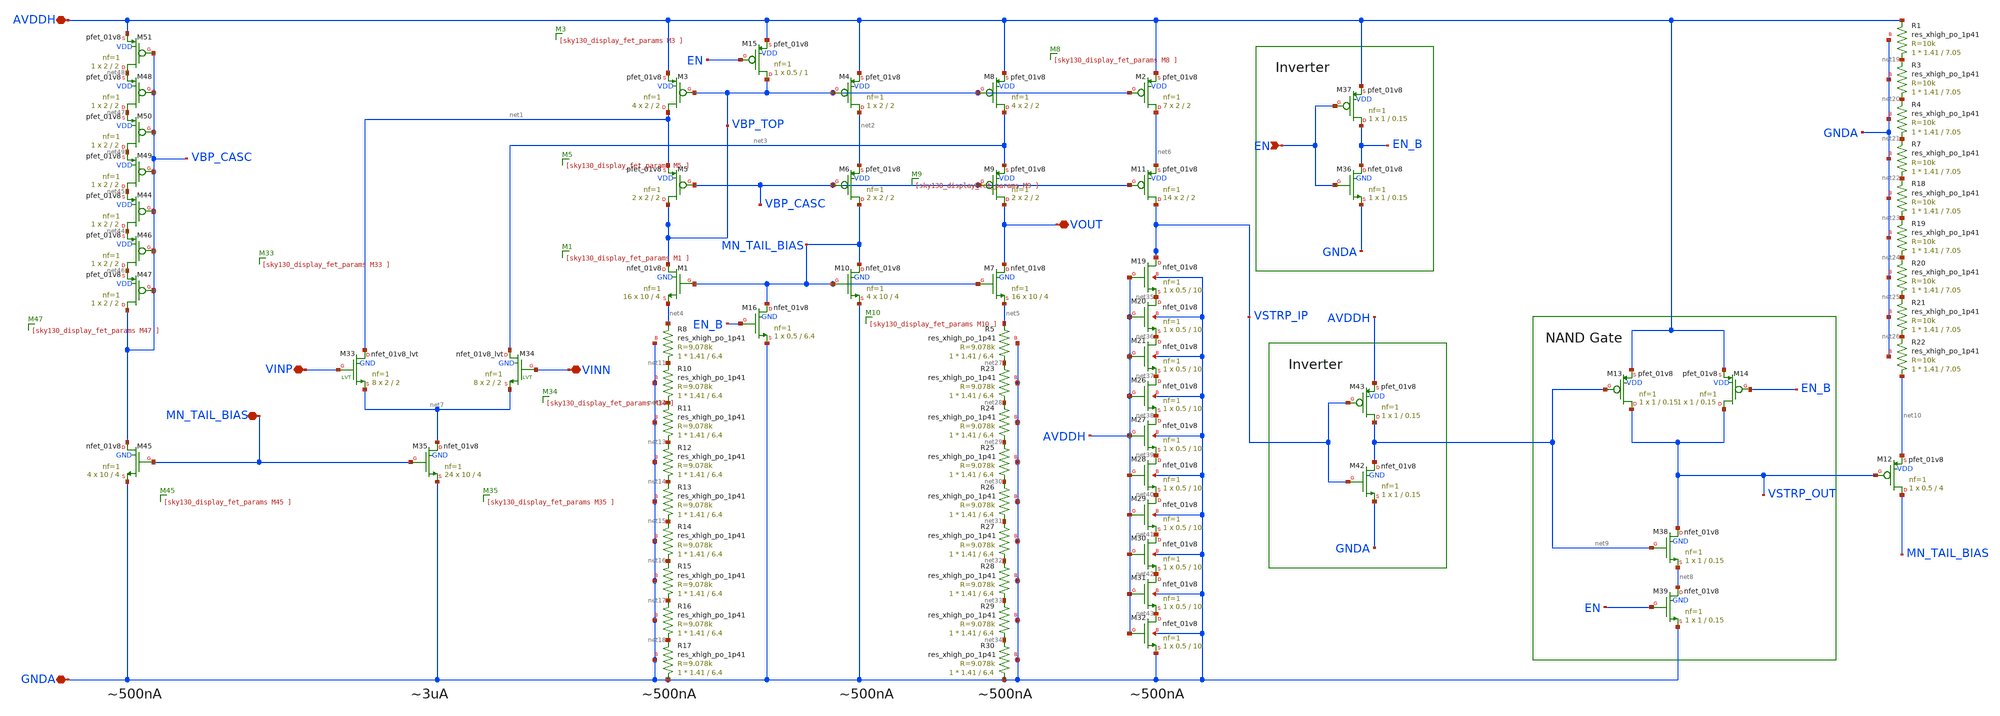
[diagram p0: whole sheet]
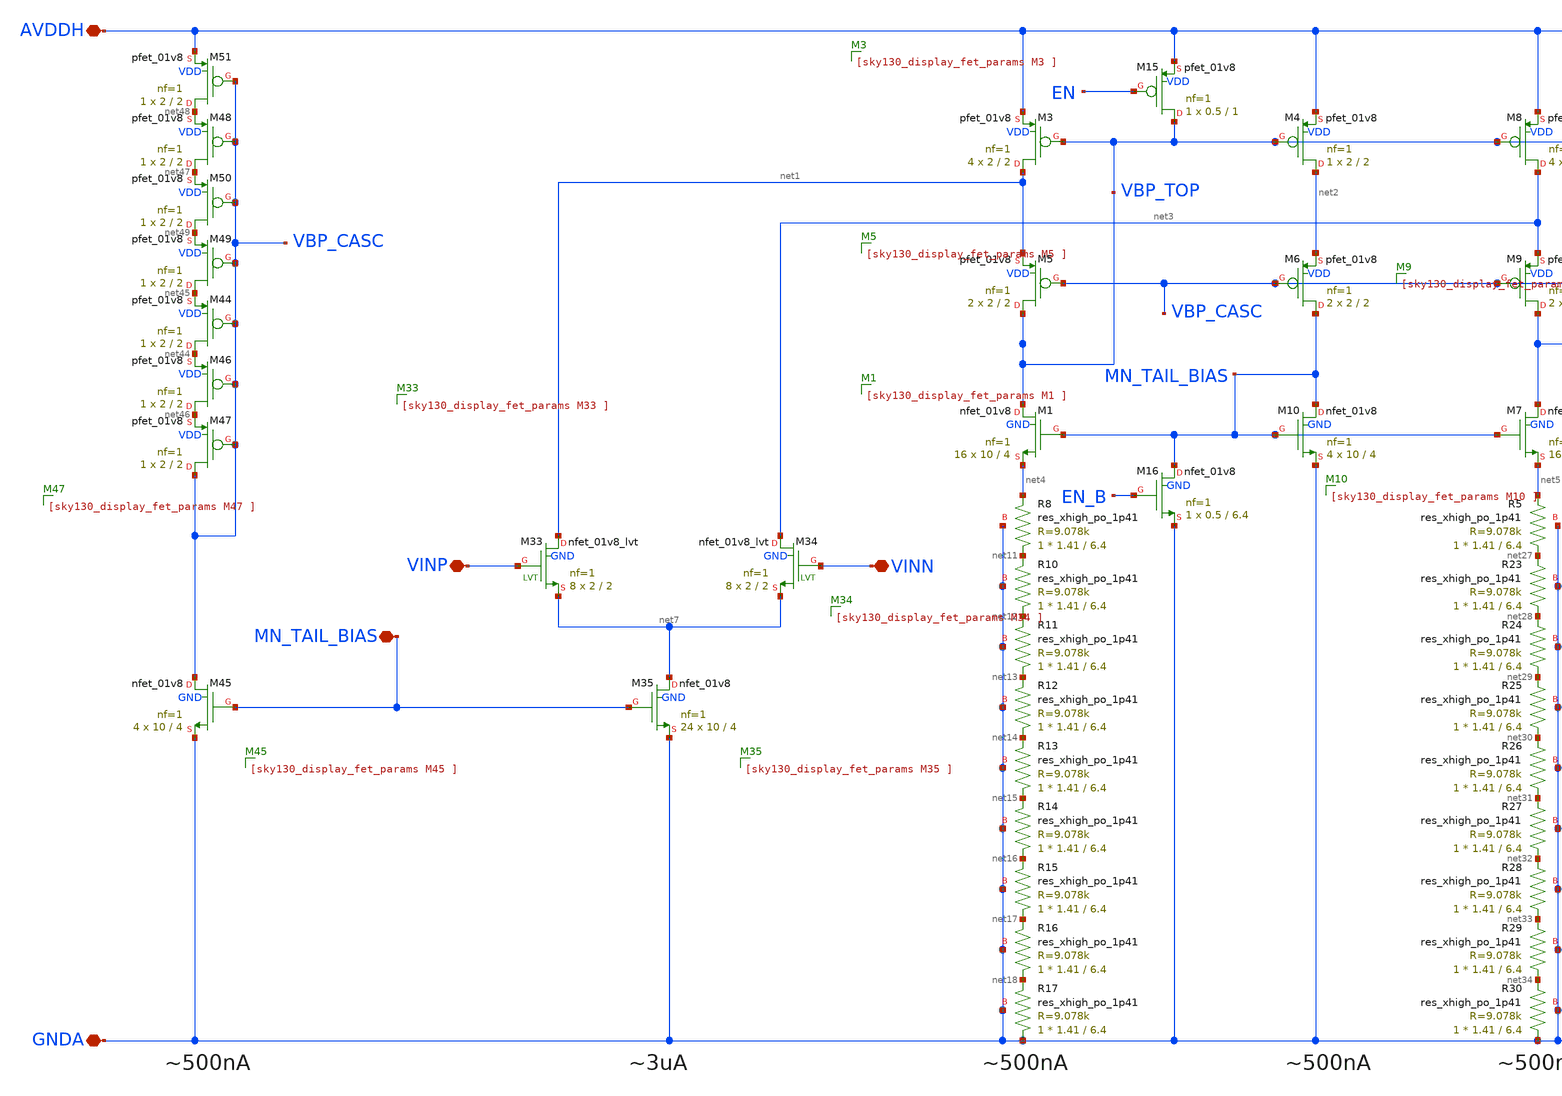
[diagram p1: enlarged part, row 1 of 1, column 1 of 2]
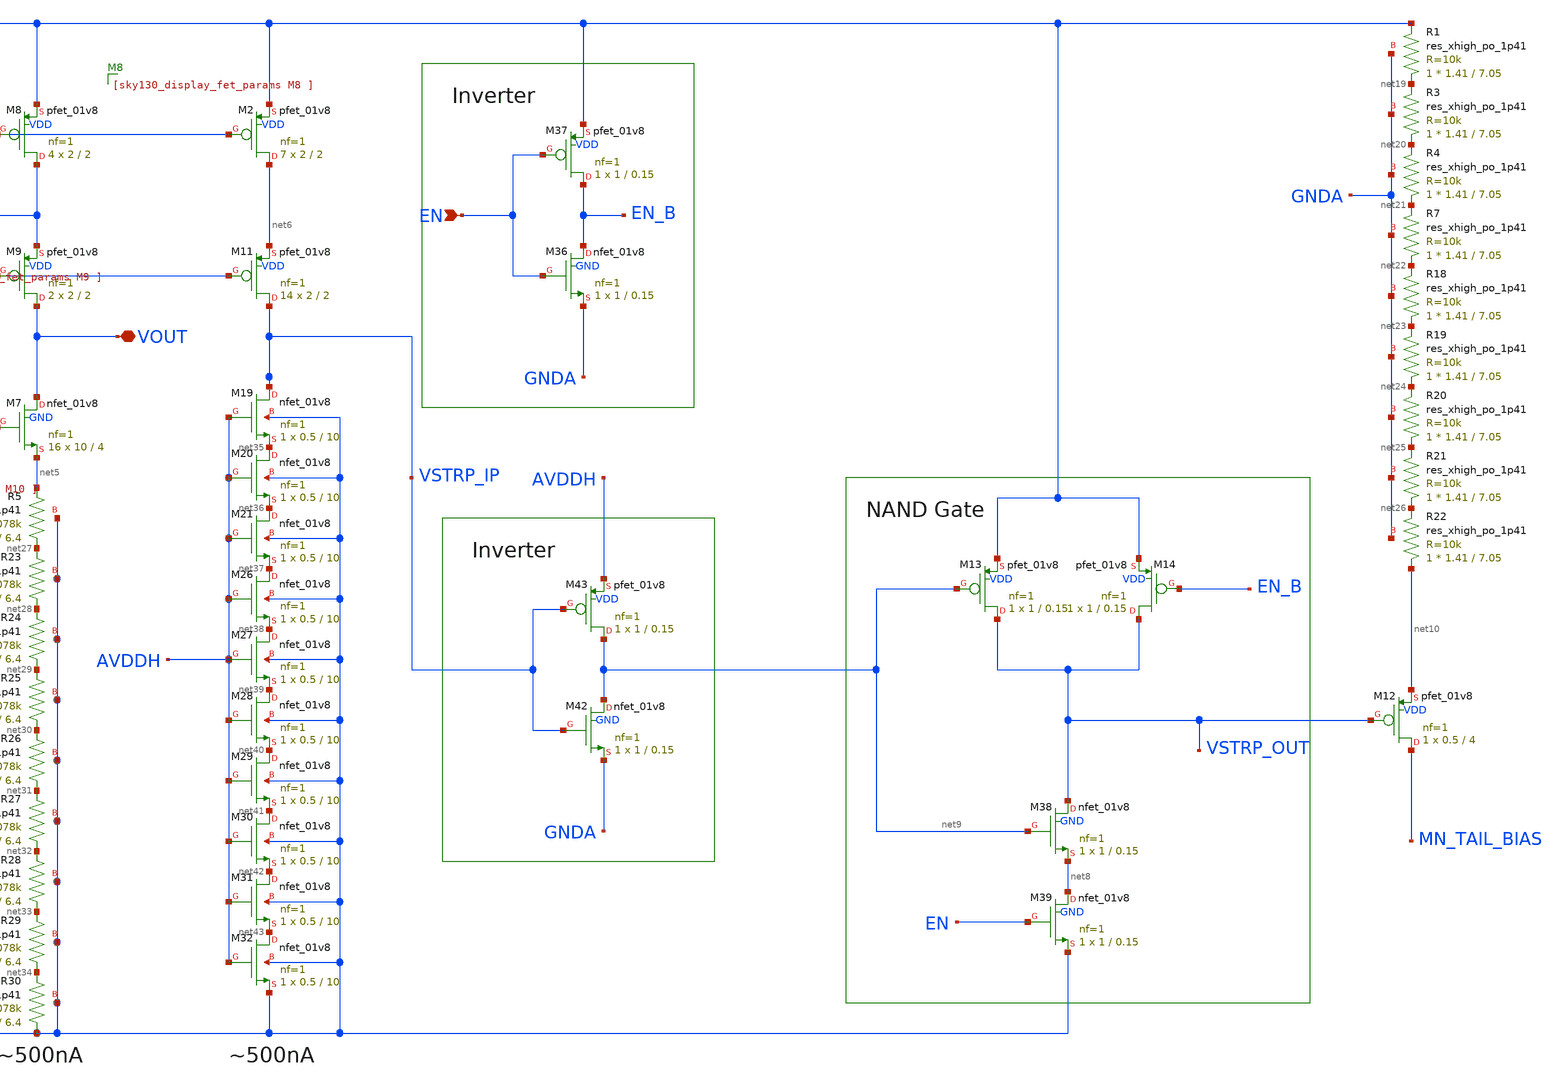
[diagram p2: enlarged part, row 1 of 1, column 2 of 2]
** sch_path: OTAs/NMOS_FoldedCasc_SE_OTA_IntBias/SCH/OTA_Gm_Cell_v2.sch
**.subckt OTA_Gm_Cell_v2 AVDDH GNDA VOUT MN_TAIL_BIAS EN VINP VINN
*.iopin AVDDH
*.iopin GNDA
*.iopin VOUT
*.iopin MN_TAIL_BIAS
*.ipin EN
*.iopin VINP
*.iopin VINN
XM1 VBP_TOP MN_TAIL_BIAS net4 GND sky130_fd_pr__nfet_01v8 L=4 W=10 nf=1 ad='int((1 + 1)/2) * 10 / 1 * 0.29'
+ as='int((1 + 2)/2) * 10 / 1 * 0.29' pd='2*int((1 + 1)/2) * (10 / 1 + 0.29)' ps='2*int((1 + 2)/2) * (10 / 1 + 0.29)'
+ nrd='0.29 / 10 ' nrs='0.29 / 10 ' sa=0 sb=0 sd=0 mult=16 m=16
XM3 net1 VBP_TOP AVDDH VDD sky130_fd_pr__pfet_01v8 L=2 W=2 nf=1 ad='int((1 + 1)/2) * 2 / 1 * 0.29' as='int((1 + 2)/2) * 2 / 1 * 0.29'
+ pd='2*int((1 + 1)/2) * (2 / 1 + 0.29)' ps='2*int((1 + 2)/2) * (2 / 1 + 0.29)' nrd='0.29 / 2 ' nrs='0.29 / 2 '
+ sa=0 sb=0 sd=0 mult=4 m=4
XM4 net2 VBP_TOP AVDDH VDD sky130_fd_pr__pfet_01v8 L=2 W=2 nf=1 ad='int((1 + 1)/2) * 2 / 1 * 0.29' as='int((1 + 2)/2) * 2 / 1 * 0.29'
+ pd='2*int((1 + 1)/2) * (2 / 1 + 0.29)' ps='2*int((1 + 2)/2) * (2 / 1 + 0.29)' nrd='0.29 / 2 ' nrs='0.29 / 2 '
+ sa=0 sb=0 sd=0 mult=1 m=1
XM5 VBP_TOP VBP_CASC net1 VDD sky130_fd_pr__pfet_01v8 L=2 W=2 nf=1 ad='int((1 + 1)/2) * 2 / 1 * 0.29'
+ as='int((1 + 2)/2) * 2 / 1 * 0.29' pd='2*int((1 + 1)/2) * (2 / 1 + 0.29)' ps='2*int((1 + 2)/2) * (2 / 1 + 0.29)'
+ nrd='0.29 / 2 ' nrs='0.29 / 2 ' sa=0 sb=0 sd=0 mult=2 m=2
XM6 MN_TAIL_BIAS VBP_CASC net2 VDD sky130_fd_pr__pfet_01v8 L=2 W=2 nf=1 ad='int((1 + 1)/2) * 2 / 1 * 0.29'
+ as='int((1 + 2)/2) * 2 / 1 * 0.29' pd='2*int((1 + 1)/2) * (2 / 1 + 0.29)' ps='2*int((1 + 2)/2) * (2 / 1 + 0.29)'
+ nrd='0.29 / 2 ' nrs='0.29 / 2 ' sa=0 sb=0 sd=0 mult=2 m=2
XM7 VOUT MN_TAIL_BIAS net5 GND sky130_fd_pr__nfet_01v8 L=4 W=10 nf=1 ad='int((1 + 1)/2) * 10 / 1 * 0.29'
+ as='int((1 + 2)/2) * 10 / 1 * 0.29' pd='2*int((1 + 1)/2) * (10 / 1 + 0.29)' ps='2*int((1 + 2)/2) * (10 / 1 + 0.29)'
+ nrd='0.29 / 10 ' nrs='0.29 / 10 ' sa=0 sb=0 sd=0 mult=16 m=16
XM10 MN_TAIL_BIAS MN_TAIL_BIAS GNDA GND sky130_fd_pr__nfet_01v8 L=4 W=10 nf=1 ad='int((1 + 1)/2) * 10 / 1 * 0.29'
+ as='int((1 + 2)/2) * 10 / 1 * 0.29' pd='2*int((1 + 1)/2) * (10 / 1 + 0.29)' ps='2*int((1 + 2)/2) * (10 / 1 + 0.29)'
+ nrd='0.29 / 10 ' nrs='0.29 / 10 ' sa=0 sb=0 sd=0 mult=4 m=4
XM12 MN_TAIL_BIAS VSTRP_OUT net10 VDD sky130_fd_pr__pfet_01v8 L=4 W=0.5 nf=1 ad='int((1 + 1)/2) * 0.5 / 1 * 0.29'
+ as='int((1 + 2)/2) * 0.5 / 1 * 0.29' pd='2*int((1 + 1)/2) * (0.5 / 1 + 0.29)' ps='2*int((1 + 2)/2) * (0.5 / 1 + 0.29)'
+ nrd='0.29 / 0.5 ' nrs='0.29 / 0.5 ' sa=0 sb=0 sd=0 mult=1 m=1
XM15 VBP_TOP EN AVDDH VDD sky130_fd_pr__pfet_01v8 L=1 W=0.5 nf=1 ad='int((1 + 1)/2) * 0.5 / 1 * 0.29'
+ as='int((1 + 2)/2) * 0.5 / 1 * 0.29' pd='2*int((1 + 1)/2) * (0.5 / 1 + 0.29)' ps='2*int((1 + 2)/2) * (0.5 / 1 + 0.29)'
+ nrd='0.29 / 0.5 ' nrs='0.29 / 0.5 ' sa=0 sb=0 sd=0 mult=1 m=1
XM16 MN_TAIL_BIAS EN_B GNDA GND sky130_fd_pr__nfet_01v8 L=6.4 W=0.5 nf=1 ad='int((1 + 1)/2) * 0.5 / 1 * 0.29'
+ as='int((1 + 2)/2) * 0.5 / 1 * 0.29' pd='2*int((1 + 1)/2) * (0.5 / 1 + 0.29)' ps='2*int((1 + 2)/2) * (0.5 / 1 + 0.29)'
+ nrd='0.29 / 0.5 ' nrs='0.29 / 0.5 ' sa=0 sb=0 sd=0 mult=1 m=1
XM8 net3 VBP_TOP AVDDH VDD sky130_fd_pr__pfet_01v8 L=2 W=2 nf=1 ad='int((1 + 1)/2) * 2 / 1 * 0.29' as='int((1 + 2)/2) * 2 / 1 * 0.29'
+ pd='2*int((1 + 1)/2) * (2 / 1 + 0.29)' ps='2*int((1 + 2)/2) * (2 / 1 + 0.29)' nrd='0.29 / 2 ' nrs='0.29 / 2 '
+ sa=0 sb=0 sd=0 mult=4 m=4
XM9 VOUT VBP_CASC net3 VDD sky130_fd_pr__pfet_01v8 L=2 W=2 nf=1 ad='int((1 + 1)/2) * 2 / 1 * 0.29' as='int((1 + 2)/2) * 2 / 1 * 0.29'
+ pd='2*int((1 + 1)/2) * (2 / 1 + 0.29)' ps='2*int((1 + 2)/2) * (2 / 1 + 0.29)' nrd='0.29 / 2 ' nrs='0.29 / 2 '
+ sa=0 sb=0 sd=0 mult=2 m=2
XR8 net11 net4 GNDA sky130_fd_pr__res_xhigh_po_1p41 L=6.4 mult=1 m=1
XR10 net12 net11 GNDA sky130_fd_pr__res_xhigh_po_1p41 L=6.4 mult=1 m=1
XR11 net13 net12 GNDA sky130_fd_pr__res_xhigh_po_1p41 L=6.4 mult=1 m=1
XR12 net14 net13 GNDA sky130_fd_pr__res_xhigh_po_1p41 L=6.4 mult=1 m=1
XR13 net15 net14 GNDA sky130_fd_pr__res_xhigh_po_1p41 L=6.4 mult=1 m=1
XR14 net16 net15 GNDA sky130_fd_pr__res_xhigh_po_1p41 L=6.4 mult=1 m=1
XR15 net17 net16 GNDA sky130_fd_pr__res_xhigh_po_1p41 L=6.4 mult=1 m=1
XR16 net18 net17 GNDA sky130_fd_pr__res_xhigh_po_1p41 L=6.4 mult=1 m=1
XR17 GNDA net18 GNDA sky130_fd_pr__res_xhigh_po_1p41 L=6.4 mult=1 m=1
XR1 net19 AVDDH GNDA sky130_fd_pr__res_xhigh_po_1p41 L=7.05 mult=1 m=1
XR3 net20 net19 GNDA sky130_fd_pr__res_xhigh_po_1p41 L=7.05 mult=1 m=1
XR4 net21 net20 GNDA sky130_fd_pr__res_xhigh_po_1p41 L=7.05 mult=1 m=1
XR7 net22 net21 GNDA sky130_fd_pr__res_xhigh_po_1p41 L=7.05 mult=1 m=1
XR18 net23 net22 GNDA sky130_fd_pr__res_xhigh_po_1p41 L=7.05 mult=1 m=1
XR19 net24 net23 GNDA sky130_fd_pr__res_xhigh_po_1p41 L=7.05 mult=1 m=1
XR20 net25 net24 GNDA sky130_fd_pr__res_xhigh_po_1p41 L=7.05 mult=1 m=1
XR21 net26 net25 GNDA sky130_fd_pr__res_xhigh_po_1p41 L=7.05 mult=1 m=1
XR22 net10 net26 GNDA sky130_fd_pr__res_xhigh_po_1p41 L=7.05 mult=1 m=1
XR5 net27 net5 GNDA sky130_fd_pr__res_xhigh_po_1p41 L=6.4 mult=1 m=1
XR23 net28 net27 GNDA sky130_fd_pr__res_xhigh_po_1p41 L=6.4 mult=1 m=1
XR24 net29 net28 GNDA sky130_fd_pr__res_xhigh_po_1p41 L=6.4 mult=1 m=1
XR25 net30 net29 GNDA sky130_fd_pr__res_xhigh_po_1p41 L=6.4 mult=1 m=1
XR26 net31 net30 GNDA sky130_fd_pr__res_xhigh_po_1p41 L=6.4 mult=1 m=1
XR27 net32 net31 GNDA sky130_fd_pr__res_xhigh_po_1p41 L=6.4 mult=1 m=1
XR28 net33 net32 GNDA sky130_fd_pr__res_xhigh_po_1p41 L=6.4 mult=1 m=1
XR29 net34 net33 GNDA sky130_fd_pr__res_xhigh_po_1p41 L=6.4 mult=1 m=1
XR30 GNDA net34 GNDA sky130_fd_pr__res_xhigh_po_1p41 L=6.4 mult=1 m=1
XM2 net6 VBP_TOP AVDDH VDD sky130_fd_pr__pfet_01v8 L=2 W=2 nf=1 ad='int((1 + 1)/2) * 2 / 1 * 0.29' as='int((1 + 2)/2) * 2 / 1 * 0.29'
+ pd='2*int((1 + 1)/2) * (2 / 1 + 0.29)' ps='2*int((1 + 2)/2) * (2 / 1 + 0.29)' nrd='0.29 / 2 ' nrs='0.29 / 2 '
+ sa=0 sb=0 sd=0 mult=7 m=7
XM11 VSTRP_IP VBP_CASC net6 VDD sky130_fd_pr__pfet_01v8 L=2 W=2 nf=1 ad='int((1 + 1)/2) * 2 / 1 * 0.29'
+ as='int((1 + 2)/2) * 2 / 1 * 0.29' pd='2*int((1 + 1)/2) * (2 / 1 + 0.29)' ps='2*int((1 + 2)/2) * (2 / 1 + 0.29)'
+ nrd='0.29 / 2 ' nrs='0.29 / 2 ' sa=0 sb=0 sd=0 mult=14 m=14
XM19 VSTRP_IP AVDDH net35 GNDA sky130_fd_pr__nfet_01v8 L=10 W=0.5 nf=1 ad='int((1 + 1)/2) * 0.5 / 1 * 0.29'
+ as='int((1 + 2)/2) * 0.5 / 1 * 0.29' pd='2*int((1 + 1)/2) * (0.5 / 1 + 0.29)' ps='2*int((1 + 2)/2) * (0.5 / 1 + 0.29)'
+ nrd='0.29 / 0.5 ' nrs='0.29 / 0.5 ' sa=0 sb=0 sd=0 mult=1 m=1
XM20 net35 AVDDH net36 GNDA sky130_fd_pr__nfet_01v8 L=10 W=0.5 nf=1 ad='int((1 + 1)/2) * 0.5 / 1 * 0.29'
+ as='int((1 + 2)/2) * 0.5 / 1 * 0.29' pd='2*int((1 + 1)/2) * (0.5 / 1 + 0.29)' ps='2*int((1 + 2)/2) * (0.5 / 1 + 0.29)'
+ nrd='0.29 / 0.5 ' nrs='0.29 / 0.5 ' sa=0 sb=0 sd=0 mult=1 m=1
XM21 net36 AVDDH net37 GNDA sky130_fd_pr__nfet_01v8 L=10 W=0.5 nf=1 ad='int((1 + 1)/2) * 0.5 / 1 * 0.29'
+ as='int((1 + 2)/2) * 0.5 / 1 * 0.29' pd='2*int((1 + 1)/2) * (0.5 / 1 + 0.29)' ps='2*int((1 + 2)/2) * (0.5 / 1 + 0.29)'
+ nrd='0.29 / 0.5 ' nrs='0.29 / 0.5 ' sa=0 sb=0 sd=0 mult=1 m=1
XM26 net37 AVDDH net38 GNDA sky130_fd_pr__nfet_01v8 L=10 W=0.5 nf=1 ad='int((1 + 1)/2) * 0.5 / 1 * 0.29'
+ as='int((1 + 2)/2) * 0.5 / 1 * 0.29' pd='2*int((1 + 1)/2) * (0.5 / 1 + 0.29)' ps='2*int((1 + 2)/2) * (0.5 / 1 + 0.29)'
+ nrd='0.29 / 0.5 ' nrs='0.29 / 0.5 ' sa=0 sb=0 sd=0 mult=1 m=1
XM27 net38 AVDDH net39 GNDA sky130_fd_pr__nfet_01v8 L=10 W=0.5 nf=1 ad='int((1 + 1)/2) * 0.5 / 1 * 0.29'
+ as='int((1 + 2)/2) * 0.5 / 1 * 0.29' pd='2*int((1 + 1)/2) * (0.5 / 1 + 0.29)' ps='2*int((1 + 2)/2) * (0.5 / 1 + 0.29)'
+ nrd='0.29 / 0.5 ' nrs='0.29 / 0.5 ' sa=0 sb=0 sd=0 mult=1 m=1
XM28 net39 AVDDH net40 GNDA sky130_fd_pr__nfet_01v8 L=10 W=0.5 nf=1 ad='int((1 + 1)/2) * 0.5 / 1 * 0.29'
+ as='int((1 + 2)/2) * 0.5 / 1 * 0.29' pd='2*int((1 + 1)/2) * (0.5 / 1 + 0.29)' ps='2*int((1 + 2)/2) * (0.5 / 1 + 0.29)'
+ nrd='0.29 / 0.5 ' nrs='0.29 / 0.5 ' sa=0 sb=0 sd=0 mult=1 m=1
XM29 net40 AVDDH net41 GNDA sky130_fd_pr__nfet_01v8 L=10 W=0.5 nf=1 ad='int((1 + 1)/2) * 0.5 / 1 * 0.29'
+ as='int((1 + 2)/2) * 0.5 / 1 * 0.29' pd='2*int((1 + 1)/2) * (0.5 / 1 + 0.29)' ps='2*int((1 + 2)/2) * (0.5 / 1 + 0.29)'
+ nrd='0.29 / 0.5 ' nrs='0.29 / 0.5 ' sa=0 sb=0 sd=0 mult=1 m=1
XM30 net41 AVDDH net42 GNDA sky130_fd_pr__nfet_01v8 L=10 W=0.5 nf=1 ad='int((1 + 1)/2) * 0.5 / 1 * 0.29'
+ as='int((1 + 2)/2) * 0.5 / 1 * 0.29' pd='2*int((1 + 1)/2) * (0.5 / 1 + 0.29)' ps='2*int((1 + 2)/2) * (0.5 / 1 + 0.29)'
+ nrd='0.29 / 0.5 ' nrs='0.29 / 0.5 ' sa=0 sb=0 sd=0 mult=1 m=1
XM31 net42 AVDDH net43 GNDA sky130_fd_pr__nfet_01v8 L=10 W=0.5 nf=1 ad='int((1 + 1)/2) * 0.5 / 1 * 0.29'
+ as='int((1 + 2)/2) * 0.5 / 1 * 0.29' pd='2*int((1 + 1)/2) * (0.5 / 1 + 0.29)' ps='2*int((1 + 2)/2) * (0.5 / 1 + 0.29)'
+ nrd='0.29 / 0.5 ' nrs='0.29 / 0.5 ' sa=0 sb=0 sd=0 mult=1 m=1
XM32 net43 AVDDH GNDA GNDA sky130_fd_pr__nfet_01v8 L=10 W=0.5 nf=1 ad='int((1 + 1)/2) * 0.5 / 1 * 0.29'
+ as='int((1 + 2)/2) * 0.5 / 1 * 0.29' pd='2*int((1 + 1)/2) * (0.5 / 1 + 0.29)' ps='2*int((1 + 2)/2) * (0.5 / 1 + 0.29)'
+ nrd='0.29 / 0.5 ' nrs='0.29 / 0.5 ' sa=0 sb=0 sd=0 mult=1 m=1
XM33 net1 VINP net7 GND sky130_fd_pr__nfet_01v8_lvt L=2 W=2 nf=1 ad='int((1 + 1)/2) * 2 / 1 * 0.29' as='int((1 + 2)/2) * 2 / 1 * 0.29'
+ pd='2*int((1 + 1)/2) * (2 / 1 + 0.29)' ps='2*int((1 + 2)/2) * (2 / 1 + 0.29)' nrd='0.29 / 2 ' nrs='0.29 / 2 '
+ sa=0 sb=0 sd=0 mult=8 m=8
XM34 net3 VINN net7 GND sky130_fd_pr__nfet_01v8_lvt L=2 W=2 nf=1 ad='int((1 + 1)/2) * 2 / 1 * 0.29' as='int((1 + 2)/2) * 2 / 1 * 0.29'
+ pd='2*int((1 + 1)/2) * (2 / 1 + 0.29)' ps='2*int((1 + 2)/2) * (2 / 1 + 0.29)' nrd='0.29 / 2 ' nrs='0.29 / 2 '
+ sa=0 sb=0 sd=0 mult=8 m=8
XM35 net7 MN_TAIL_BIAS GNDA GND sky130_fd_pr__nfet_01v8 L=4 W=10 nf=1 ad='int((1 + 1)/2) * 10 / 1 * 0.29'
+ as='int((1 + 2)/2) * 10 / 1 * 0.29' pd='2*int((1 + 1)/2) * (10 / 1 + 0.29)' ps='2*int((1 + 2)/2) * (10 / 1 + 0.29)'
+ nrd='0.29 / 10 ' nrs='0.29 / 10 ' sa=0 sb=0 sd=0 mult=24 m=24
XM36 EN_B EN GNDA GND sky130_fd_pr__nfet_01v8 L=0.15 W=1 nf=1 ad='int((1 + 1)/2) * 1 / 1 * 0.29' as='int((1 + 2)/2) * 1 / 1 * 0.29'
+ pd='2*int((1 + 1)/2) * (1 / 1 + 0.29)' ps='2*int((1 + 2)/2) * (1 / 1 + 0.29)' nrd='0.29 / 1 ' nrs='0.29 / 1 '
+ sa=0 sb=0 sd=0 mult=1 m=1
XM37 EN_B EN AVDDH VDD sky130_fd_pr__pfet_01v8 L=0.15 W=1 nf=1 ad='int((1 + 1)/2) * 1 / 1 * 0.29' as='int((1 + 2)/2) * 1 / 1 * 0.29'
+ pd='2*int((1 + 1)/2) * (1 / 1 + 0.29)' ps='2*int((1 + 2)/2) * (1 / 1 + 0.29)' nrd='0.29 / 1 ' nrs='0.29 / 1 '
+ sa=0 sb=0 sd=0 mult=1 m=1
XM38 VSTRP_OUT net9 net8 GND sky130_fd_pr__nfet_01v8 L=0.15 W=1 nf=1 ad='int((1 + 1)/2) * 1 / 1 * 0.29'
+ as='int((1 + 2)/2) * 1 / 1 * 0.29' pd='2*int((1 + 1)/2) * (1 / 1 + 0.29)' ps='2*int((1 + 2)/2) * (1 / 1 + 0.29)'
+ nrd='0.29 / 1 ' nrs='0.29 / 1 ' sa=0 sb=0 sd=0 mult=1 m=1
XM39 net8 EN GNDA GND sky130_fd_pr__nfet_01v8 L=0.15 W=1 nf=1 ad='int((1 + 1)/2) * 1 / 1 * 0.29' as='int((1 + 2)/2) * 1 / 1 * 0.29'
+ pd='2*int((1 + 1)/2) * (1 / 1 + 0.29)' ps='2*int((1 + 2)/2) * (1 / 1 + 0.29)' nrd='0.29 / 1 ' nrs='0.29 / 1 '
+ sa=0 sb=0 sd=0 mult=1 m=1
XM42 net9 VSTRP_IP GNDA GND sky130_fd_pr__nfet_01v8 L=0.15 W=1 nf=1 ad='int((1 + 1)/2) * 1 / 1 * 0.29'
+ as='int((1 + 2)/2) * 1 / 1 * 0.29' pd='2*int((1 + 1)/2) * (1 / 1 + 0.29)' ps='2*int((1 + 2)/2) * (1 / 1 + 0.29)'
+ nrd='0.29 / 1 ' nrs='0.29 / 1 ' sa=0 sb=0 sd=0 mult=1 m=1
XM43 net9 VSTRP_IP AVDDH VDD sky130_fd_pr__pfet_01v8 L=0.15 W=1 nf=1 ad='int((1 + 1)/2) * 1 / 1 * 0.29'
+ as='int((1 + 2)/2) * 1 / 1 * 0.29' pd='2*int((1 + 1)/2) * (1 / 1 + 0.29)' ps='2*int((1 + 2)/2) * (1 / 1 + 0.29)'
+ nrd='0.29 / 1 ' nrs='0.29 / 1 ' sa=0 sb=0 sd=0 mult=1 m=1
XM44 net44 VBP_CASC net45 VDD sky130_fd_pr__pfet_01v8 L=2 W=2 nf=1 ad='int((1 + 1)/2) * 2 / 1 * 0.29'
+ as='int((1 + 2)/2) * 2 / 1 * 0.29' pd='2*int((1 + 1)/2) * (2 / 1 + 0.29)' ps='2*int((1 + 2)/2) * (2 / 1 + 0.29)'
+ nrd='0.29 / 2 ' nrs='0.29 / 2 ' sa=0 sb=0 sd=0 mult=1 m=1
XM45 VBP_CASC MN_TAIL_BIAS GNDA GND sky130_fd_pr__nfet_01v8 L=4 W=10 nf=1 ad='int((1 + 1)/2) * 10 / 1 * 0.29'
+ as='int((1 + 2)/2) * 10 / 1 * 0.29' pd='2*int((1 + 1)/2) * (10 / 1 + 0.29)' ps='2*int((1 + 2)/2) * (10 / 1 + 0.29)'
+ nrd='0.29 / 10 ' nrs='0.29 / 10 ' sa=0 sb=0 sd=0 mult=4 m=4
XM46 net46 VBP_CASC net44 VDD sky130_fd_pr__pfet_01v8 L=2 W=2 nf=1 ad='int((1 + 1)/2) * 2 / 1 * 0.29'
+ as='int((1 + 2)/2) * 2 / 1 * 0.29' pd='2*int((1 + 1)/2) * (2 / 1 + 0.29)' ps='2*int((1 + 2)/2) * (2 / 1 + 0.29)'
+ nrd='0.29 / 2 ' nrs='0.29 / 2 ' sa=0 sb=0 sd=0 mult=1 m=1
XM47 VBP_CASC VBP_CASC net46 VDD sky130_fd_pr__pfet_01v8 L=2 W=2 nf=1 ad='int((1 + 1)/2) * 2 / 1 * 0.29'
+ as='int((1 + 2)/2) * 2 / 1 * 0.29' pd='2*int((1 + 1)/2) * (2 / 1 + 0.29)' ps='2*int((1 + 2)/2) * (2 / 1 + 0.29)'
+ nrd='0.29 / 2 ' nrs='0.29 / 2 ' sa=0 sb=0 sd=0 mult=1 m=1
XM48 net47 VBP_CASC net48 VDD sky130_fd_pr__pfet_01v8 L=2 W=2 nf=1 ad='int((1 + 1)/2) * 2 / 1 * 0.29'
+ as='int((1 + 2)/2) * 2 / 1 * 0.29' pd='2*int((1 + 1)/2) * (2 / 1 + 0.29)' ps='2*int((1 + 2)/2) * (2 / 1 + 0.29)'
+ nrd='0.29 / 2 ' nrs='0.29 / 2 ' sa=0 sb=0 sd=0 mult=1 m=1
XM49 net45 VBP_CASC net49 VDD sky130_fd_pr__pfet_01v8 L=2 W=2 nf=1 ad='int((1 + 1)/2) * 2 / 1 * 0.29'
+ as='int((1 + 2)/2) * 2 / 1 * 0.29' pd='2*int((1 + 1)/2) * (2 / 1 + 0.29)' ps='2*int((1 + 2)/2) * (2 / 1 + 0.29)'
+ nrd='0.29 / 2 ' nrs='0.29 / 2 ' sa=0 sb=0 sd=0 mult=1 m=1
XM50 net49 VBP_CASC net47 VDD sky130_fd_pr__pfet_01v8 L=2 W=2 nf=1 ad='int((1 + 1)/2) * 2 / 1 * 0.29'
+ as='int((1 + 2)/2) * 2 / 1 * 0.29' pd='2*int((1 + 1)/2) * (2 / 1 + 0.29)' ps='2*int((1 + 2)/2) * (2 / 1 + 0.29)'
+ nrd='0.29 / 2 ' nrs='0.29 / 2 ' sa=0 sb=0 sd=0 mult=1 m=1
XM51 net48 VBP_CASC AVDDH VDD sky130_fd_pr__pfet_01v8 L=2 W=2 nf=1 ad='int((1 + 1)/2) * 2 / 1 * 0.29'
+ as='int((1 + 2)/2) * 2 / 1 * 0.29' pd='2*int((1 + 1)/2) * (2 / 1 + 0.29)' ps='2*int((1 + 2)/2) * (2 / 1 + 0.29)'
+ nrd='0.29 / 2 ' nrs='0.29 / 2 ' sa=0 sb=0 sd=0 mult=1 m=1
XM13 VSTRP_OUT net9 AVDDH VDD sky130_fd_pr__pfet_01v8 L=0.15 W=1 nf=1 ad='int((1 + 1)/2) * 1 / 1 * 0.29'
+ as='int((1 + 2)/2) * 1 / 1 * 0.29' pd='2*int((1 + 1)/2) * (1 / 1 + 0.29)' ps='2*int((1 + 2)/2) * (1 / 1 + 0.29)'
+ nrd='0.29 / 1 ' nrs='0.29 / 1 ' sa=0 sb=0 sd=0 mult=1 m=1
XM14 VSTRP_OUT EN_B AVDDH VDD sky130_fd_pr__pfet_01v8 L=0.15 W=1 nf=1 ad='int((1 + 1)/2) * 1 / 1 * 0.29'
+ as='int((1 + 2)/2) * 1 / 1 * 0.29' pd='2*int((1 + 1)/2) * (1 / 1 + 0.29)' ps='2*int((1 + 2)/2) * (1 / 1 + 0.29)'
+ nrd='0.29 / 1 ' nrs='0.29 / 1 ' sa=0 sb=0 sd=0 mult=1 m=1
**.ends
.end
